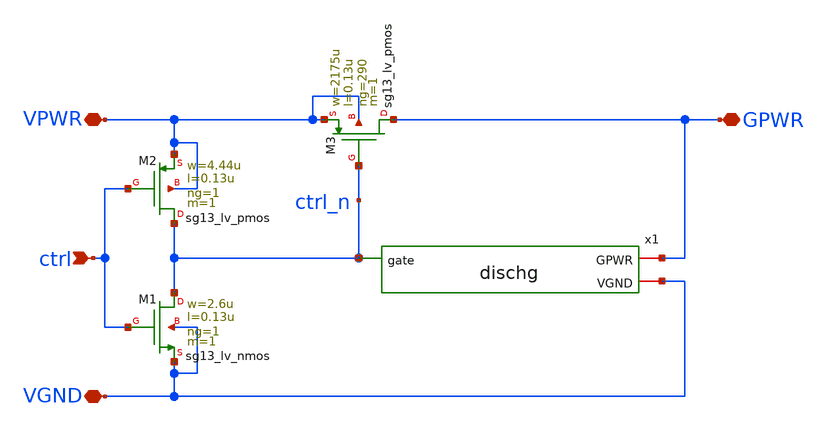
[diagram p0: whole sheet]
** sch_path: ihp-sg13cmos5l/libs.tech/xschem/hm_analog/power_gate.sch
**.subckt power_gate ctrl VPWR VGND GPWR
*.ipin ctrl
*.iopin VPWR
*.iopin VGND
*.iopin GPWR
XM1 ctrl_n ctrl VGND VGND sg13_lv_nmos w=2.6u l=0.13u ng=1 m=1 mm_ok=1
XM2 ctrl_n ctrl VPWR VPWR sg13_lv_pmos w=4.44u l=0.13u ng=1 m=1 mm_ok=1
XM3 GPWR ctrl_n VPWR VPWR sg13_lv_pmos w=2175u l=0.13u ng=290 m=1 mm_ok=1
x1 VGND GPWR ctrl_n dischg
**.ends

* expanding   symbol:
*+  /home/designer/shared/hm-openpdk-library/ihp-sg13cmos5l/libs.tech/xschem/hm_analog/dischg.sym # of pins=3
** sym_path: ihp-sg13cmos5l/libs.tech/xschem/hm_analog/dischg.sym
** sch_path: ihp-sg13cmos5l/libs.tech/xschem/hm_analog/dischg.sch
.subckt dischg VGND GPWR gate
*.iopin GPWR
*.iopin VGND
*.ipin gate
XM1 GPWR gate net6 GPWR sg13_lv_nmos w=0.50u l=0.65u ng=1 m=1 mm_ok=1
XM2 net6 gate net5 net6 sg13_lv_nmos w=0.50u l=0.65u ng=1 m=1 mm_ok=1
XM3 net5 gate net4 net5 sg13_lv_nmos w=0.50u l=0.65u ng=1 m=1 mm_ok=1
XM4 net4 gate VGND net4 sg13_lv_nmos w=0.50u l=0.65u ng=1 m=1 mm_ok=1
XM5 GPWR gate net3 GPWR sg13_lv_nmos w=0.50u l=0.65u ng=1 m=1 mm_ok=1
XM6 net3 gate net2 net3 sg13_lv_nmos w=0.50u l=0.65u ng=1 m=1 mm_ok=1
XM7 net2 gate net1 net2 sg13_lv_nmos w=0.50u l=0.65u ng=1 m=1 mm_ok=1
XM8 net1 gate VGND net1 sg13_lv_nmos w=0.50u l=0.65u ng=1 m=1 mm_ok=1
.ends

.end
